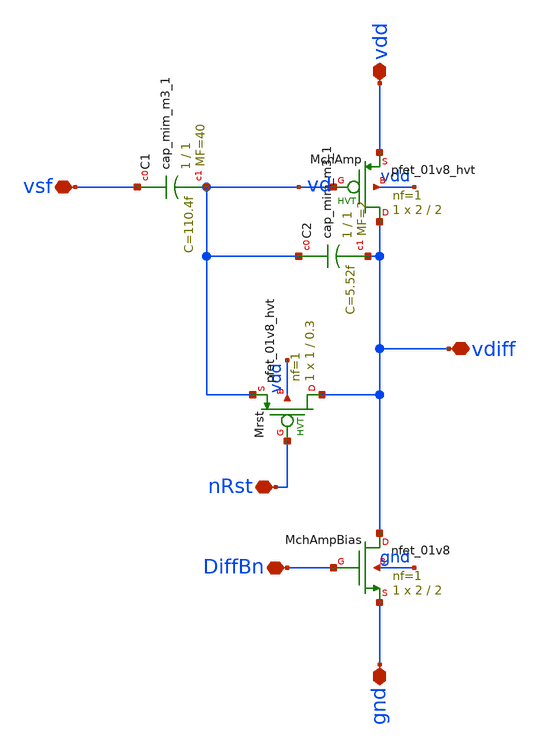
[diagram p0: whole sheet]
** sch_path: analog/xschem/PixelChangeAmplifier.sch
**.subckt PixelChangeAmplifier DiffBn vsf vdd gnd vdiff nRst
*.iopin DiffBn
*.iopin vsf
*.iopin vdd
*.iopin gnd
*.iopin vdiff
*.iopin nRst
XC1 vsf vd sky130_fd_pr__cap_mim_m3_1 W=1 L=1 MF=40 m=40
XC2 vd vdiff sky130_fd_pr__cap_mim_m3_1 W=1 L=1 MF=2 m=2
XMchAmpBias vdiff DiffBn gnd gnd sky130_fd_pr__nfet_01v8 L=2 W=2 nf=1 ad='int((1 + 1)/2) * 2 / 1 * 0.29'
+ as='int((1 + 2)/2) * 2 / 1 * 0.29' pd='2*int((1 + 1)/2) * (2 / 1 + 0.29)' ps='2*int((1 + 2)/2) * (2 / 1 + 0.29)'
+ nrd='0.29 / 2 ' nrs='0.29 / 2 ' sa=0 sb=0 sd=0 mult=1 m=1
XMrst vdiff nRst vd vdd sky130_fd_pr__pfet_01v8_hvt L=0.3 W=1 nf=1 ad='int((1 + 1)/2) * 1 / 1 * 0.29'
+ as='int((1 + 2)/2) * 1 / 1 * 0.29' pd='2*int((1 + 1)/2) * (1 / 1 + 0.29)' ps='2*int((1 + 2)/2) * (1 / 1 + 0.29)'
+ nrd='0.29 / 1 ' nrs='0.29 / 1 ' sa=0 sb=0 sd=0 mult=1 m=1
XMchAmp vdiff vd vdd vdd sky130_fd_pr__pfet_01v8_hvt L=2 W=2 nf=1 ad='int((1 + 1)/2) * 2 / 1 * 0.29'
+ as='int((1 + 2)/2) * 2 / 1 * 0.29' pd='2*int((1 + 1)/2) * (2 / 1 + 0.29)' ps='2*int((1 + 2)/2) * (2 / 1 + 0.29)'
+ nrd='0.29 / 2 ' nrs='0.29 / 2 ' sa=0 sb=0 sd=0 mult=1 m=1
**.ends
.end
